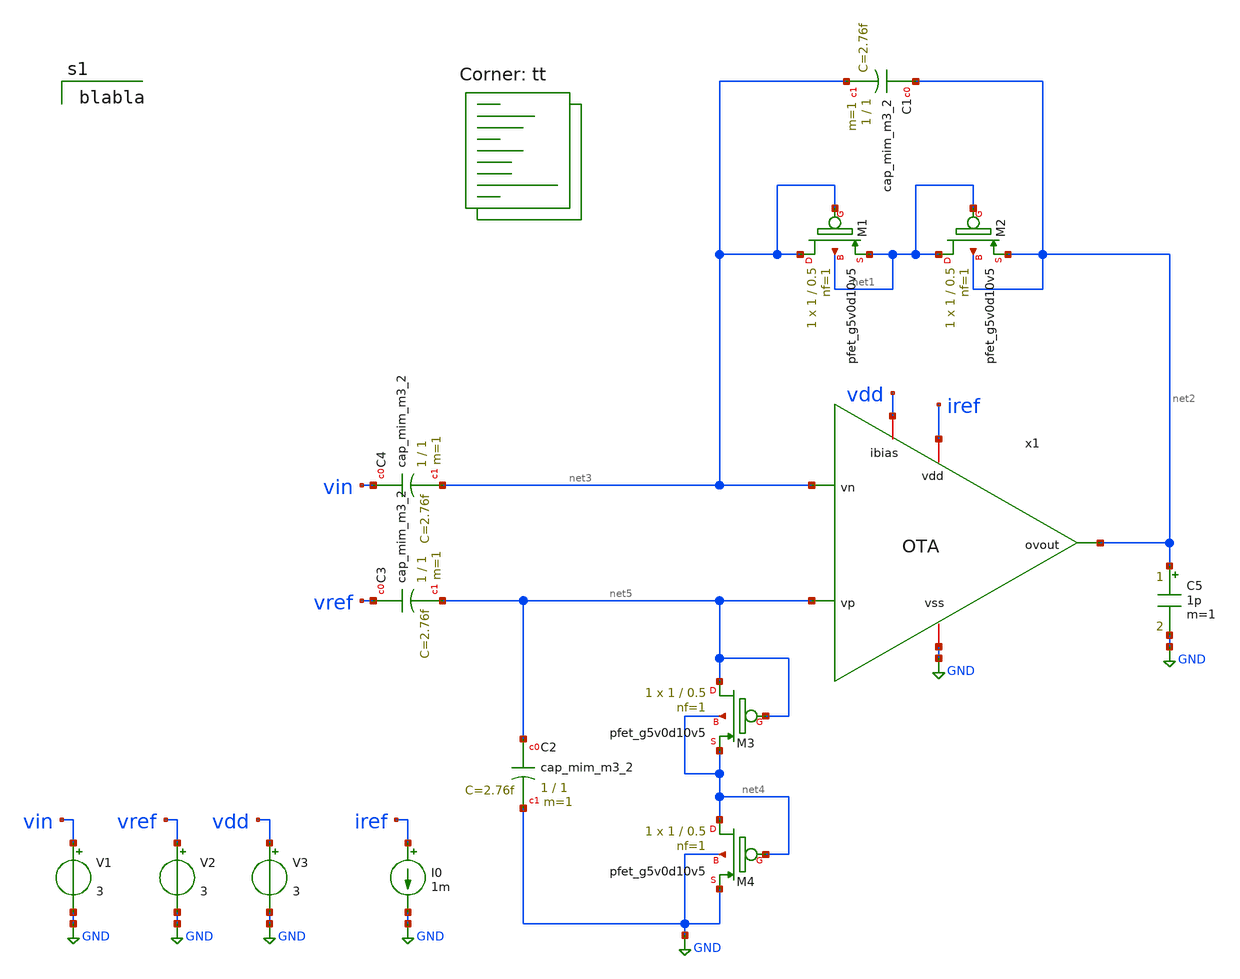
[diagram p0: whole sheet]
** sch_path: xschem/LNA.sch
**.subckt LNA
XM1 net3 net3 net1 net1 sky130_fd_pr__pfet_g5v0d10v5 L=0.5 W=1 nf=1 ad='int((nf+1)/2) * W/nf * 0.29'
+ as='int((nf+2)/2) * W/nf * 0.29' pd='2*int((nf+1)/2) * (W/nf + 0.29)' ps='2*int((nf+2)/2) * (W/nf + 0.29)'
+ nrd='0.29 / W' nrs='0.29 / W' sa=0 sb=0 sd=0 mult=1 m=1
XM2 net1 net1 net2 net2 sky130_fd_pr__pfet_g5v0d10v5 L=0.5 W=1 nf=1 ad='int((nf+1)/2) * W/nf * 0.29'
+ as='int((nf+2)/2) * W/nf * 0.29' pd='2*int((nf+1)/2) * (W/nf + 0.29)' ps='2*int((nf+2)/2) * (W/nf + 0.29)'
+ nrd='0.29 / W' nrs='0.29 / W' sa=0 sb=0 sd=0 mult=1 m=1
XM3 net5 net5 net4 net4 sky130_fd_pr__pfet_g5v0d10v5 L=0.5 W=1 nf=1 ad='int((nf+1)/2) * W/nf * 0.29'
+ as='int((nf+2)/2) * W/nf * 0.29' pd='2*int((nf+1)/2) * (W/nf + 0.29)' ps='2*int((nf+2)/2) * (W/nf + 0.29)'
+ nrd='0.29 / W' nrs='0.29 / W' sa=0 sb=0 sd=0 mult=1 m=1
XM4 net4 net4 GND GND sky130_fd_pr__pfet_g5v0d10v5 L=0.5 W=1 nf=1 ad='int((nf+1)/2) * W/nf * 0.29' as='int((nf+2)/2) * W/nf * 0.29'
+ pd='2*int((nf+1)/2) * (W/nf + 0.29)' ps='2*int((nf+2)/2) * (W/nf + 0.29)' nrd='0.29 / W' nrs='0.29 / W'
+ sa=0 sb=0 sd=0 mult=1 m=1
XC1 net2 net3 sky130_fd_pr__cap_mim_m3_2 W=1 L=1 MF=1 m=1
XC2 net5 GND sky130_fd_pr__cap_mim_m3_2 W=1 L=1 MF=1 m=1
XC3 vref net5 sky130_fd_pr__cap_mim_m3_2 W=1 L=1 MF=1 m=1
XC4 vin net3 sky130_fd_pr__cap_mim_m3_2 W=1 L=1 MF=1 m=1
C5 net2 GND 1p m=1
V1 vin GND 3
I0 iref GND 1m
V2 vref GND 3
V3 vdd GND 3
x1 net2 iref GND vdd net3 net5 OTA
**** begin user architecture code

blabla

.lib $::SKYWATER_MODELS/sky130.lib.spice tt
**** end user architecture code
**.ends

* expanding   symbol:  /home/william/projects/sky130_vbl_ip__LNA/xschem/OTA.sym # of pins=6
** sym_path: xschem/OTA.sym
** sch_path: xschem/OTA.sch
.subckt OTA ovout vdd vss ibias vn vp
*.iopin ibias
*.iopin vdd
*.iopin vss
*.ipin vp
*.ipin vn
*.opin ovout
XM5a net2 vp net1 vdd sky130_fd_pr__pfet_g5v0d10v5 L=0.5 W=80 nf=1 ad='int((nf+1)/2) * W/nf * 0.29' as='int((nf+2)/2) * W/nf * 0.29'
+ pd='2*int((nf+1)/2) * (W/nf + 0.29)' ps='2*int((nf+2)/2) * (W/nf + 0.29)' nrd='0.29 / W' nrs='0.29 / W'
+ sa=0 sb=0 sd=0 mult=1 m=1
XM5b net3 vn net1 vdd sky130_fd_pr__pfet_g5v0d10v5 L=0.5 W=80 nf=1 ad='int((nf+1)/2) * W/nf * 0.29' as='int((nf+2)/2) * W/nf * 0.29'
+ pd='2*int((nf+1)/2) * (W/nf + 0.29)' ps='2*int((nf+2)/2) * (W/nf + 0.29)' nrd='0.29 / W' nrs='0.29 / W'
+ sa=0 sb=0 sd=0 mult=1 m=1
XM4b net2 net2 vss vss sky130_fd_pr__nfet_g5v0d10v5 L=4 W=1 nf=1 ad='int((nf+1)/2) * W/nf * 0.29' as='int((nf+2)/2) * W/nf * 0.29'
+ pd='2*int((nf+1)/2) * (W/nf + 0.29)' ps='2*int((nf+2)/2) * (W/nf + 0.29)' nrd='0.29 / W' nrs='0.29 / W'
+ sa=0 sb=0 sd=0 mult=1 m=1
XM4c net3 net3 vss vss sky130_fd_pr__nfet_g5v0d10v5 L=4 W=1 nf=1 ad='int((nf+1)/2) * W/nf * 0.29' as='int((nf+2)/2) * W/nf * 0.29'
+ pd='2*int((nf+1)/2) * (W/nf + 0.29)' ps='2*int((nf+2)/2) * (W/nf + 0.29)' nrd='0.29 / W' nrs='0.29 / W'
+ sa=0 sb=0 sd=0 mult=1 m=1
XM4a net5 net2 vss vss sky130_fd_pr__nfet_g5v0d10v5 L=4 W=1 nf=1 ad='int((nf+1)/2) * W/nf * 0.29' as='int((nf+2)/2) * W/nf * 0.29'
+ pd='2*int((nf+1)/2) * (W/nf + 0.29)' ps='2*int((nf+2)/2) * (W/nf + 0.29)' nrd='0.29 / W' nrs='0.29 / W'
+ sa=0 sb=0 sd=0 mult=1 m=1
XM4d net7 net3 vss vss sky130_fd_pr__nfet_g5v0d10v5 L=4 W=1 nf=1 ad='int((nf+1)/2) * W/nf * 0.29' as='int((nf+2)/2) * W/nf * 0.29'
+ pd='2*int((nf+1)/2) * (W/nf + 0.29)' ps='2*int((nf+2)/2) * (W/nf + 0.29)' nrd='0.29 / W' nrs='0.29 / W'
+ sa=0 sb=0 sd=0 mult=1 m=1
XM1a net4 net4 vdd vdd sky130_fd_pr__pfet_g5v0d10v5 L=1 W=0.6 nf=1 ad='int((nf+1)/2) * W/nf * 0.29' as='int((nf+2)/2) * W/nf * 0.29'
+ pd='2*int((nf+1)/2) * (W/nf + 0.29)' ps='2*int((nf+2)/2) * (W/nf + 0.29)' nrd='0.29 / W' nrs='0.29 / W'
+ sa=0 sb=0 sd=0 mult=1 m=1
XM1b net8 net4 vdd vdd sky130_fd_pr__pfet_g5v0d10v5 L=1 W=0.6 nf=1 ad='int((nf+1)/2) * W/nf * 0.29' as='int((nf+2)/2) * W/nf * 0.29'
+ pd='2*int((nf+1)/2) * (W/nf + 0.29)' ps='2*int((nf+2)/2) * (W/nf + 0.29)' nrd='0.29 / W' nrs='0.29 / W'
+ sa=0 sb=0 sd=0 mult=1 m=1
XM7 ibias ibias vdd vdd sky130_fd_pr__pfet_g5v0d10v5 L=2 W=2 nf=1 ad='int((nf+1)/2) * W/nf * 0.29' as='int((nf+2)/2) * W/nf * 0.29'
+ pd='2*int((nf+1)/2) * (W/nf + 0.29)' ps='2*int((nf+2)/2) * (W/nf + 0.29)' nrd='0.29 / W' nrs='0.29 / W'
+ sa=0 sb=0 sd=0 mult=1 m=1
XM6 net1 ibias vdd vdd sky130_fd_pr__pfet_g5v0d10v5 L=2 W=2 nf=1 ad='int((nf+1)/2) * W/nf * 0.29' as='int((nf+2)/2) * W/nf * 0.29'
+ pd='2*int((nf+1)/2) * (W/nf + 0.29)' ps='2*int((nf+2)/2) * (W/nf + 0.29)' nrd='0.29 / W' nrs='0.29 / W'
+ sa=0 sb=0 sd=0 mult=1 m=1
XM3a net6 net6 net5 vss sky130_fd_pr__nfet_g5v0d10v5 L=4 W=1 nf=1 ad='int((nf+1)/2) * W/nf * 0.29' as='int((nf+2)/2) * W/nf * 0.29'
+ pd='2*int((nf+1)/2) * (W/nf + 0.29)' ps='2*int((nf+2)/2) * (W/nf + 0.29)' nrd='0.29 / W' nrs='0.29 / W'
+ sa=0 sb=0 sd=0 mult=1 m=1
XM2a net6 net6 net4 vdd sky130_fd_pr__pfet_g5v0d10v5 L=1 W=0.6 nf=1 ad='int((nf+1)/2) * W/nf * 0.29'
+ as='int((nf+2)/2) * W/nf * 0.29' pd='2*int((nf+1)/2) * (W/nf + 0.29)' ps='2*int((nf+2)/2) * (W/nf + 0.29)'
+ nrd='0.29 / W' nrs='0.29 / W' sa=0 sb=0 sd=0 mult=1 m=1
XM2b ovout ovout net8 vdd sky130_fd_pr__pfet_g5v0d10v5 L=1 W=0.6 nf=1 ad='int((nf+1)/2) * W/nf * 0.29'
+ as='int((nf+2)/2) * W/nf * 0.29' pd='2*int((nf+1)/2) * (W/nf + 0.29)' ps='2*int((nf+2)/2) * (W/nf + 0.29)'
+ nrd='0.29 / W' nrs='0.29 / W' sa=0 sb=0 sd=0 mult=1 m=1
XM3b ovout ovout net7 vss sky130_fd_pr__nfet_g5v0d10v5 L=4 W=1 nf=1 ad='int((nf+1)/2) * W/nf * 0.29'
+ as='int((nf+2)/2) * W/nf * 0.29' pd='2*int((nf+1)/2) * (W/nf + 0.29)' ps='2*int((nf+2)/2) * (W/nf + 0.29)'
+ nrd='0.29 / W' nrs='0.29 / W' sa=0 sb=0 sd=0 mult=1 m=1
.ends

.GLOBAL GND
.end
